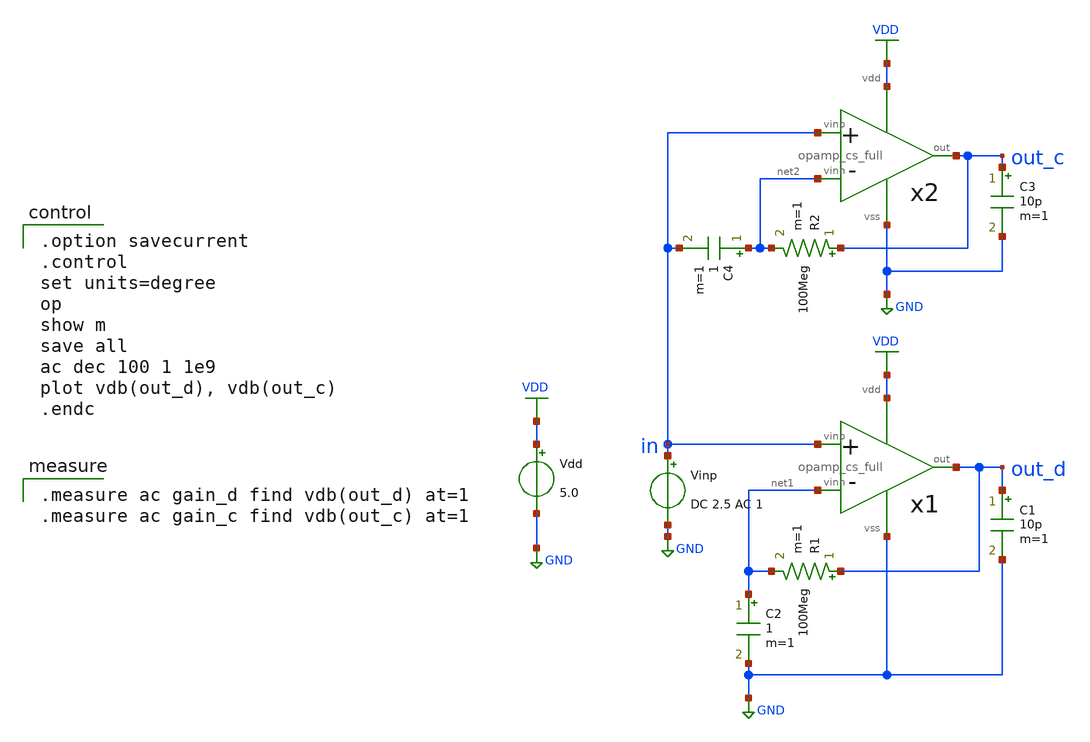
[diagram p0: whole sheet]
** sch_path: member_project/GroupWork/Team_Ando/dokunira/sch/opamp_cs_full_cmrr.sch
**.subckt opamp_cs_full_cmrr
Vdd VDD GND 5.0
Vinp in GND DC 2.5 AC 1
C1 out_d GND 10p m=1
R1 out_d net1 100Meg m=1
C2 net1 GND 1 m=1
C3 out_c GND 10p m=1
R2 out_c net2 100Meg m=1
C4 net2 in 1 m=1
x1 in net1 out_d VDD GND opamp_cs_full
x2 in net2 out_c VDD GND opamp_cs_full
**** begin user architecture code

.option savecurrent
.control
set units=degree
op
show m
save all
ac dec 100 1 1e9
plot vdb(out_d), vdb(out_c)
.endc


.measure ac gain_d find vdb(out_d) at=1
.measure ac gain_c find vdb(out_c) at=1

 .include $::LIB/mos.lib
.include $::LIB/passive.lib
.include $::LIB/diode.lib
**** end user architecture code
**.ends

* expanding   symbol:  opamp_cs_full.sym # of pins=5
** sym_path: member_project/GroupWork/Team_Ando/dokunira/sch/opamp_cs_full.sym
** sch_path: member_project/GroupWork/Team_Ando/dokunira/sch/opamp_cs_full.sch
.subckt opamp_cs_full vinp vinn out vdd vss
*.iopin vdd
*.iopin vss
*.ipin vinn
*.ipin vinp
*.opin out
M12 net9 net1 net6 vss nmos L=1.6u W=16u m=1
M9 net1 net3 vdd vdd pmos L=1.6u W=32u m=1
M10 net1 net1 net2 vss nmos L=1.6u W=16u m=1
M11 net2 net2 vss vss nmos L=1.6u W=16u m=1
R1 vss net4 HR_poly W=2.0 L=20
M8 net3 net3 vdd vdd pmos L=1.6u W=32u m=1
M13 net5 net3 vdd vdd pmos L=1.6u W=32u m=1
M15 net3 net5 net4 vss nmos L=1.6u W=16u m=1
M14 net5 net4 vss vss nmos L=1.6u W=16u m=1
M5 net8 net3 vdd vdd pmos L=1.6u W=64u m=1
M1 net7 vinn net8 net8 pmos L=1.6u W=128u m=1
M2 net6 vinp net8 net8 pmos L=1.6u W=128u m=1
M3 net7 net7 vss vss nmos L=1.6u W=16u m=1
M4 net6 net7 vss vss nmos L=1.6u W=16u m=1
M6 out net3 vdd vdd pmos L=1.6u W=256u m=1
M7 out net6 vss vss nmos L=1.6u W=128u m=1
C1 out net9 Poly_cap W=20 L=22
.ends

.GLOBAL GND
.GLOBAL VDD
.end
